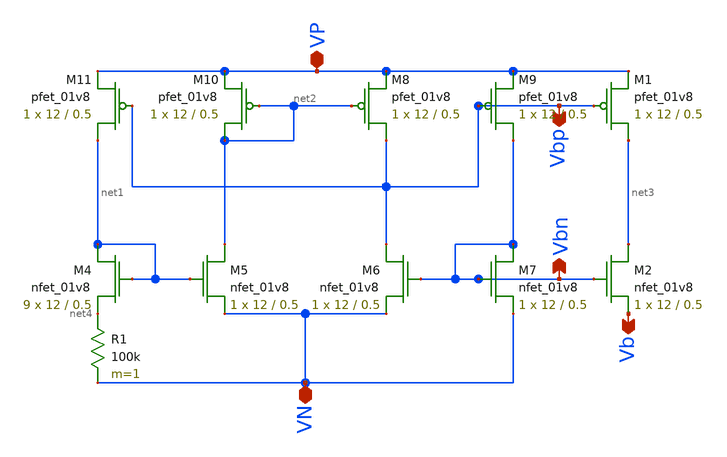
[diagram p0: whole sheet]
** sch_path: schematics/bias/current_bias.sch
**.subckt current_bias VP VN Vb Vbn Vbp
*.iopin VP
*.iopin VN
*.opin Vb
*.opin Vbn
*.opin Vbp
XM4 net1 net1 net4 GND sky130_fd_pr__nfet_01v8 L=0.5 W=12 nf=1 ad='int((nf+1)/2) * W/nf * 0.29' as='int((nf+2)/2) * W/nf * 0.29'
+ pd='2*int((nf+1)/2) * (W/nf + 0.29)' ps='2*int((nf+2)/2) * (W/nf + 0.29)' nrd='0.29 / W' nrs='0.29 / W'
+ sa=0 sb=0 sd=0 mult=9 m=9
XM5 net2 net1 VN GND sky130_fd_pr__nfet_01v8 L=0.5 W=12 nf=1 ad='int((nf+1)/2) * W/nf * 0.29' as='int((nf+2)/2) * W/nf * 0.29'
+ pd='2*int((nf+1)/2) * (W/nf + 0.29)' ps='2*int((nf+2)/2) * (W/nf + 0.29)' nrd='0.29 / W' nrs='0.29 / W'
+ sa=0 sb=0 sd=0 mult=1 m=1
XM6 Vbp Vbn VN GND sky130_fd_pr__nfet_01v8 L=0.5 W=12 nf=1 ad='int((nf+1)/2) * W/nf * 0.29' as='int((nf+2)/2) * W/nf * 0.29'
+ pd='2*int((nf+1)/2) * (W/nf + 0.29)' ps='2*int((nf+2)/2) * (W/nf + 0.29)' nrd='0.29 / W' nrs='0.29 / W'
+ sa=0 sb=0 sd=0 mult=1 m=1
XM7 Vbn Vbn VN GND sky130_fd_pr__nfet_01v8 L=0.5 W=12 nf=1 ad='int((nf+1)/2) * W/nf * 0.29' as='int((nf+2)/2) * W/nf * 0.29'
+ pd='2*int((nf+1)/2) * (W/nf + 0.29)' ps='2*int((nf+2)/2) * (W/nf + 0.29)' nrd='0.29 / W' nrs='0.29 / W'
+ sa=0 sb=0 sd=0 mult=1 m=1
R1 net4 VN 100k m=1
XM8 Vbp net2 VP VDD sky130_fd_pr__pfet_01v8 L=0.5 W=12 nf=1 ad='int((nf+1)/2) * W/nf * 0.29' as='int((nf+2)/2) * W/nf * 0.29'
+ pd='2*int((nf+1)/2) * (W/nf + 0.29)' ps='2*int((nf+2)/2) * (W/nf + 0.29)' nrd='0.29 / W' nrs='0.29 / W'
+ sa=0 sb=0 sd=0 mult=1 m=1
XM9 Vbn Vbp VP VDD sky130_fd_pr__pfet_01v8 L=0.5 W=12 nf=1 ad='int((nf+1)/2) * W/nf * 0.29' as='int((nf+2)/2) * W/nf * 0.29'
+ pd='2*int((nf+1)/2) * (W/nf + 0.29)' ps='2*int((nf+2)/2) * (W/nf + 0.29)' nrd='0.29 / W' nrs='0.29 / W'
+ sa=0 sb=0 sd=0 mult=1 m=1
XM10 net2 net2 VP VDD sky130_fd_pr__pfet_01v8 L=0.5 W=12 nf=1 ad='int((nf+1)/2) * W/nf * 0.29' as='int((nf+2)/2) * W/nf * 0.29'
+ pd='2*int((nf+1)/2) * (W/nf + 0.29)' ps='2*int((nf+2)/2) * (W/nf + 0.29)' nrd='0.29 / W' nrs='0.29 / W'
+ sa=0 sb=0 sd=0 mult=1 m=1
XM11 net1 Vbp VP VDD sky130_fd_pr__pfet_01v8 L=0.5 W=12 nf=1 ad='int((nf+1)/2) * W/nf * 0.29' as='int((nf+2)/2) * W/nf * 0.29'
+ pd='2*int((nf+1)/2) * (W/nf + 0.29)' ps='2*int((nf+2)/2) * (W/nf + 0.29)' nrd='0.29 / W' nrs='0.29 / W'
+ sa=0 sb=0 sd=0 mult=1 m=1
XM1 net3 Vbp VP VDD sky130_fd_pr__pfet_01v8 L=0.5 W=12 nf=1 ad='int((nf+1)/2) * W/nf * 0.29' as='int((nf+2)/2) * W/nf * 0.29'
+ pd='2*int((nf+1)/2) * (W/nf + 0.29)' ps='2*int((nf+2)/2) * (W/nf + 0.29)' nrd='0.29 / W' nrs='0.29 / W'
+ sa=0 sb=0 sd=0 mult=1 m=1
XM2 net3 Vbn Vb GND sky130_fd_pr__nfet_01v8 L=0.5 W=12 nf=1 ad='int((nf+1)/2) * W/nf * 0.29' as='int((nf+2)/2) * W/nf * 0.29'
+ pd='2*int((nf+1)/2) * (W/nf + 0.29)' ps='2*int((nf+2)/2) * (W/nf + 0.29)' nrd='0.29 / W' nrs='0.29 / W'
+ sa=0 sb=0 sd=0 mult=1 m=1
**.ends
.end
